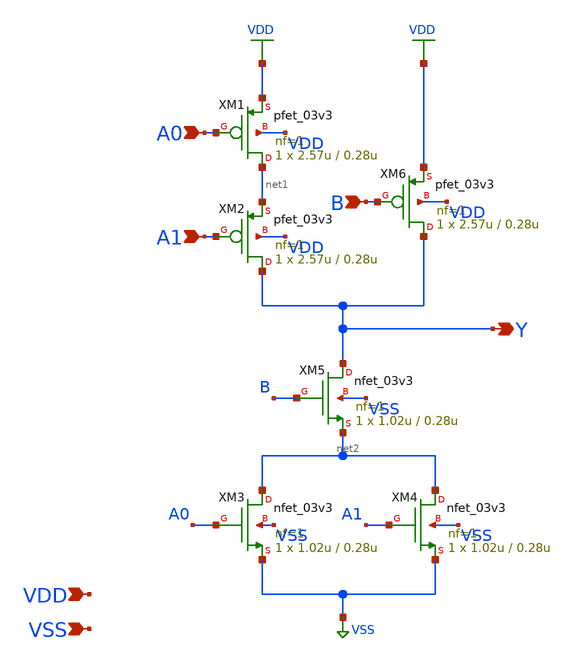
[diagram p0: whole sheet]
** sch_path: xschem/gf180mcu_ocd_sc_rt12t3v3__oai21_1.sch
**.subckt gf180mcu_ocd_sc_rt12t3v3__oai21_1 A0 A1 B Y VDD VSS
*.ipin A0
*.ipin A1
*.ipin B
*.opin Y
*.ipin VDD
*.ipin VSS
XM1 net1 A0 VDD VDD pfet_03v3 L=0.28u W=2.57u nf=1 ad='int((nf+1)/2) * W/nf * 0.18u' as='int((nf+2)/2) * W/nf * 0.18u'
+ pd='2*int((nf+1)/2) * (W/nf + 0.18u)' ps='2*int((nf+2)/2) * (W/nf + 0.18u)' nrd='0.18u / W' nrs='0.18u / W'
+ sa=0 sb=0 sd=0 m=1
XM2 Y A1 net1 VDD pfet_03v3 L=0.28u W=2.57u nf=1 ad='int((nf+1)/2) * W/nf * 0.18u' as='int((nf+2)/2) * W/nf * 0.18u'
+ pd='2*int((nf+1)/2) * (W/nf + 0.18u)' ps='2*int((nf+2)/2) * (W/nf + 0.18u)' nrd='0.18u / W' nrs='0.18u / W'
+ sa=0 sb=0 sd=0 m=1
XM3 net2 A0 VSS VSS nfet_03v3 L=0.28u W=1.02u nf=1 ad='int((nf+1)/2) * W/nf * 0.18u' as='int((nf+2)/2) * W/nf * 0.18u'
+ pd='2*int((nf+1)/2) * (W/nf + 0.18u)' ps='2*int((nf+2)/2) * (W/nf + 0.18u)' nrd='0.18u / W' nrs='0.18u / W'
+ sa=0 sb=0 sd=0 m=1
XM4 net2 A1 VSS VSS nfet_03v3 L=0.28u W=1.02u nf=1 ad='int((nf+1)/2) * W/nf * 0.18u' as='int((nf+2)/2) * W/nf * 0.18u'
+ pd='2*int((nf+1)/2) * (W/nf + 0.18u)' ps='2*int((nf+2)/2) * (W/nf + 0.18u)' nrd='0.18u / W' nrs='0.18u / W'
+ sa=0 sb=0 sd=0 m=1
XM5 Y B net2 VSS nfet_03v3 L=0.28u W=1.02u nf=1 ad='int((nf+1)/2) * W/nf * 0.18u' as='int((nf+2)/2) * W/nf * 0.18u'
+ pd='2*int((nf+1)/2) * (W/nf + 0.18u)' ps='2*int((nf+2)/2) * (W/nf + 0.18u)' nrd='0.18u / W' nrs='0.18u / W'
+ sa=0 sb=0 sd=0 m=1
XM6 Y B VDD VDD pfet_03v3 L=0.28u W=2.57u nf=1 ad='int((nf+1)/2) * W/nf * 0.18u' as='int((nf+2)/2) * W/nf * 0.18u'
+ pd='2*int((nf+1)/2) * (W/nf + 0.18u)' ps='2*int((nf+2)/2) * (W/nf + 0.18u)' nrd='0.18u / W' nrs='0.18u / W'
+ sa=0 sb=0 sd=0 m=1
**.ends
.GLOBAL VDD
.GLOBAL VSS
.end
